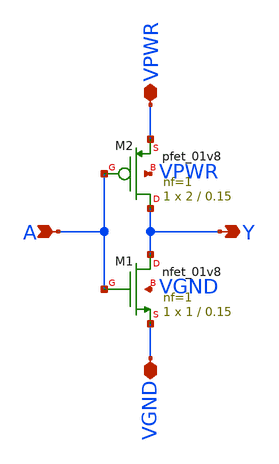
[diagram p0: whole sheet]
** sch_path: examples/sky130-inv/libs/cells/inv/schematic/inv.sch
**.subckt inv A Y VPWR VGND
*.ipin A
*.opin Y
*.iopin VPWR
*.iopin VGND
XM2 Y A VPWR VPWR sky130_fd_pr__pfet_01v8 L=0.15 W=2 nf=1 ad='int((nf+1)/2) * W/nf * 0.29' as='int((nf+2)/2) * W/nf * 0.29'
+ pd='2*int((nf+1)/2) * (W/nf + 0.29)' ps='2*int((nf+2)/2) * (W/nf + 0.29)' nrd='0.29 / W' nrs='0.29 / W'
+ sa=0 sb=0 sd=0 mult=1 m=1
XM1 Y A VGND VGND sky130_fd_pr__nfet_01v8 L=0.15 W=1 nf=1 ad='int((1 + 1)/2) * 1 / 1 * 0.29' as='int((1 + 2)/2) * 1 / 1 * 0.29'
+ pd='2*int((1 + 1)/2) * (1 / 1 + 0.29)' ps='2*int((1 + 2)/2) * (1 / 1 + 0.29)' nrd='0.29 / 1 ' nrs='0.29 / 1 '
+ sa=0 sb=0 sd=0 mult=1 m=1
**.ends
.end
